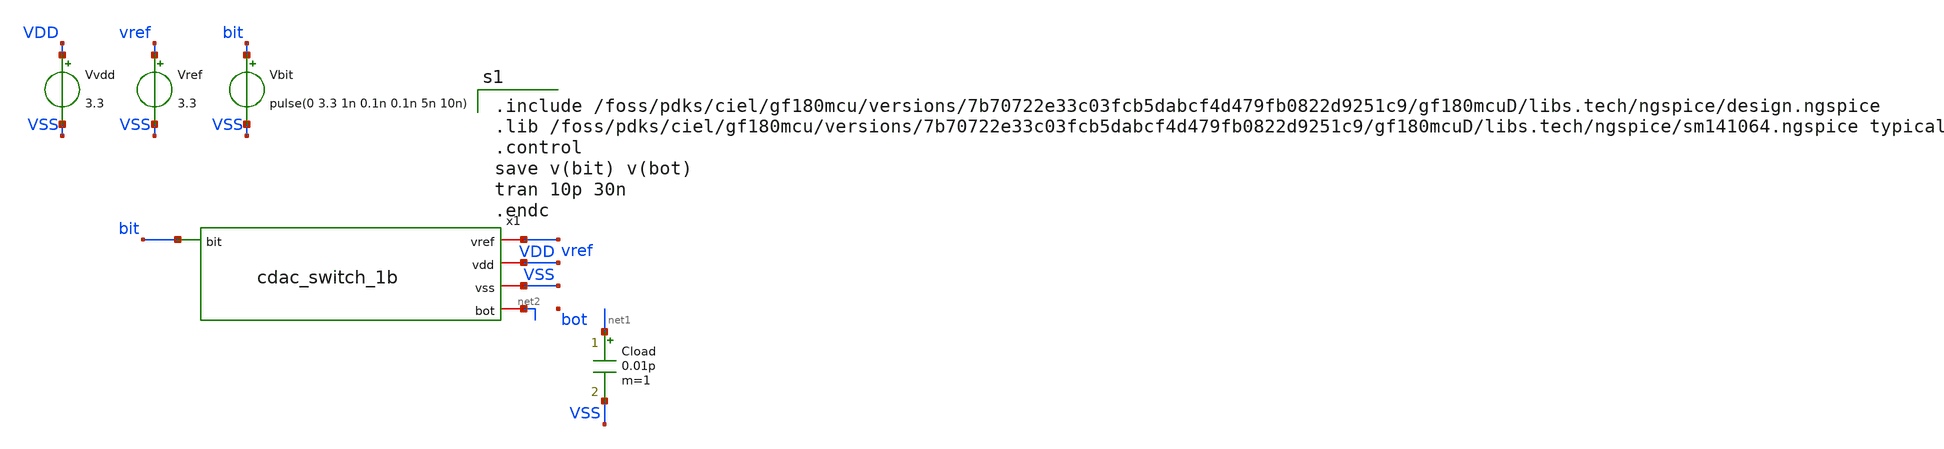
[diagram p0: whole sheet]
** sch_path: xschem/sar_adc/blocks/cdac/testbench/tb_cdac_switch_1b.sch
**.subckt tb_cdac_switch_1b
x1 bit vref VDD VSS net2 cdac_switch_1b
Vvdd VDD VSS 3.3
Vref vref VSS 3.3
Vbit bit VSS pulse(0 3.3 1n 0.1n 0.1n 5n 10n)
Cload net1 VSS 0.01p m=1
**** begin user architecture code

.include /foss/pdks/ciel/gf180mcu/versions/7b70722e33c03fcb5dabcf4d479fb0822d9251c9/gf180mcuD/libs.tech/ngspice/design.ngspice
.lib /foss/pdks/ciel/gf180mcu/versions/7b70722e33c03fcb5dabcf4d479fb0822d9251c9/gf180mcuD/libs.tech/ngspice/sm141064.ngspice typical
.control
save v(bit) v(bot)
tran 10p 30n
.endc

**** end user architecture code
**.ends

* expanding   symbol:  sar_adc/blocks/cdac/cdac_switch_1b.sym # of pins=5
** sym_path: xschem/sar_adc/blocks/cdac/cdac_switch_1b.sym
** sch_path: xschem/sar_adc/blocks/cdac/cdac_switch_1b.sch
.subckt cdac_switch_1b bit vref vdd vss bot
*.iopin vdd
*.iopin vss
*.iopin vref
*.ipin bit
*.iopin bot
*.iopin vdd
*.iopin vss
XM1 bit_b bit vdd vdd pfet_03v3 L=0.28u W=1u nf=1 ad='int((nf+1)/2) * W/nf * 0.18u' as='int((nf+2)/2) * W/nf * 0.18u'
+ pd='2*int((nf+1)/2) * (W/nf + 0.18u)' ps='2*int((nf+2)/2) * (W/nf + 0.18u)' nrd='0.18u / W' nrs='0.18u / W'
+ sa=0 sb=0 sd=0 m=1
XM2 bit_b bit vss vss nfet_03v3 L=0.28u W=0.5u nf=1 ad='int((nf+1)/2) * W/nf * 0.18u' as='int((nf+2)/2) * W/nf * 0.18u'
+ pd='2*int((nf+1)/2) * (W/nf + 0.18u)' ps='2*int((nf+2)/2) * (W/nf + 0.18u)' nrd='0.18u / W' nrs='0.18u / W'
+ sa=0 sb=0 sd=0 m=1
XM3 bot bit_b vref vdd pfet_03v3 L=0.28u W=20u nf=1 ad='int((nf+1)/2) * W/nf * 0.18u' as='int((nf+2)/2) * W/nf * 0.18u'
+ pd='2*int((nf+1)/2) * (W/nf + 0.18u)' ps='2*int((nf+2)/2) * (W/nf + 0.18u)' nrd='0.18u / W' nrs='0.18u / W'
+ sa=0 sb=0 sd=0 m=1
XM4 vref bit bot vss nfet_03v3 L=0.28u W=10u nf=1 ad='int((nf+1)/2) * W/nf * 0.18u' as='int((nf+2)/2) * W/nf * 0.18u'
+ pd='2*int((nf+1)/2) * (W/nf + 0.18u)' ps='2*int((nf+2)/2) * (W/nf + 0.18u)' nrd='0.18u / W' nrs='0.18u / W'
+ sa=0 sb=0 sd=0 m=1
XM5 bot bit vss vdd pfet_03v3 L=0.28u W=20u nf=1 ad='int((nf+1)/2) * W/nf * 0.18u' as='int((nf+2)/2) * W/nf * 0.18u'
+ pd='2*int((nf+1)/2) * (W/nf + 0.18u)' ps='2*int((nf+2)/2) * (W/nf + 0.18u)' nrd='0.18u / W' nrs='0.18u / W'
+ sa=0 sb=0 sd=0 m=1
XM6 vss bit_b bot vss nfet_03v3 L=0.28u W=10u nf=1 ad='int((nf+1)/2) * W/nf * 0.18u' as='int((nf+2)/2) * W/nf * 0.18u'
+ pd='2*int((nf+1)/2) * (W/nf + 0.18u)' ps='2*int((nf+2)/2) * (W/nf + 0.18u)' nrd='0.18u / W' nrs='0.18u / W'
+ sa=0 sb=0 sd=0 m=1
.ends

.end
